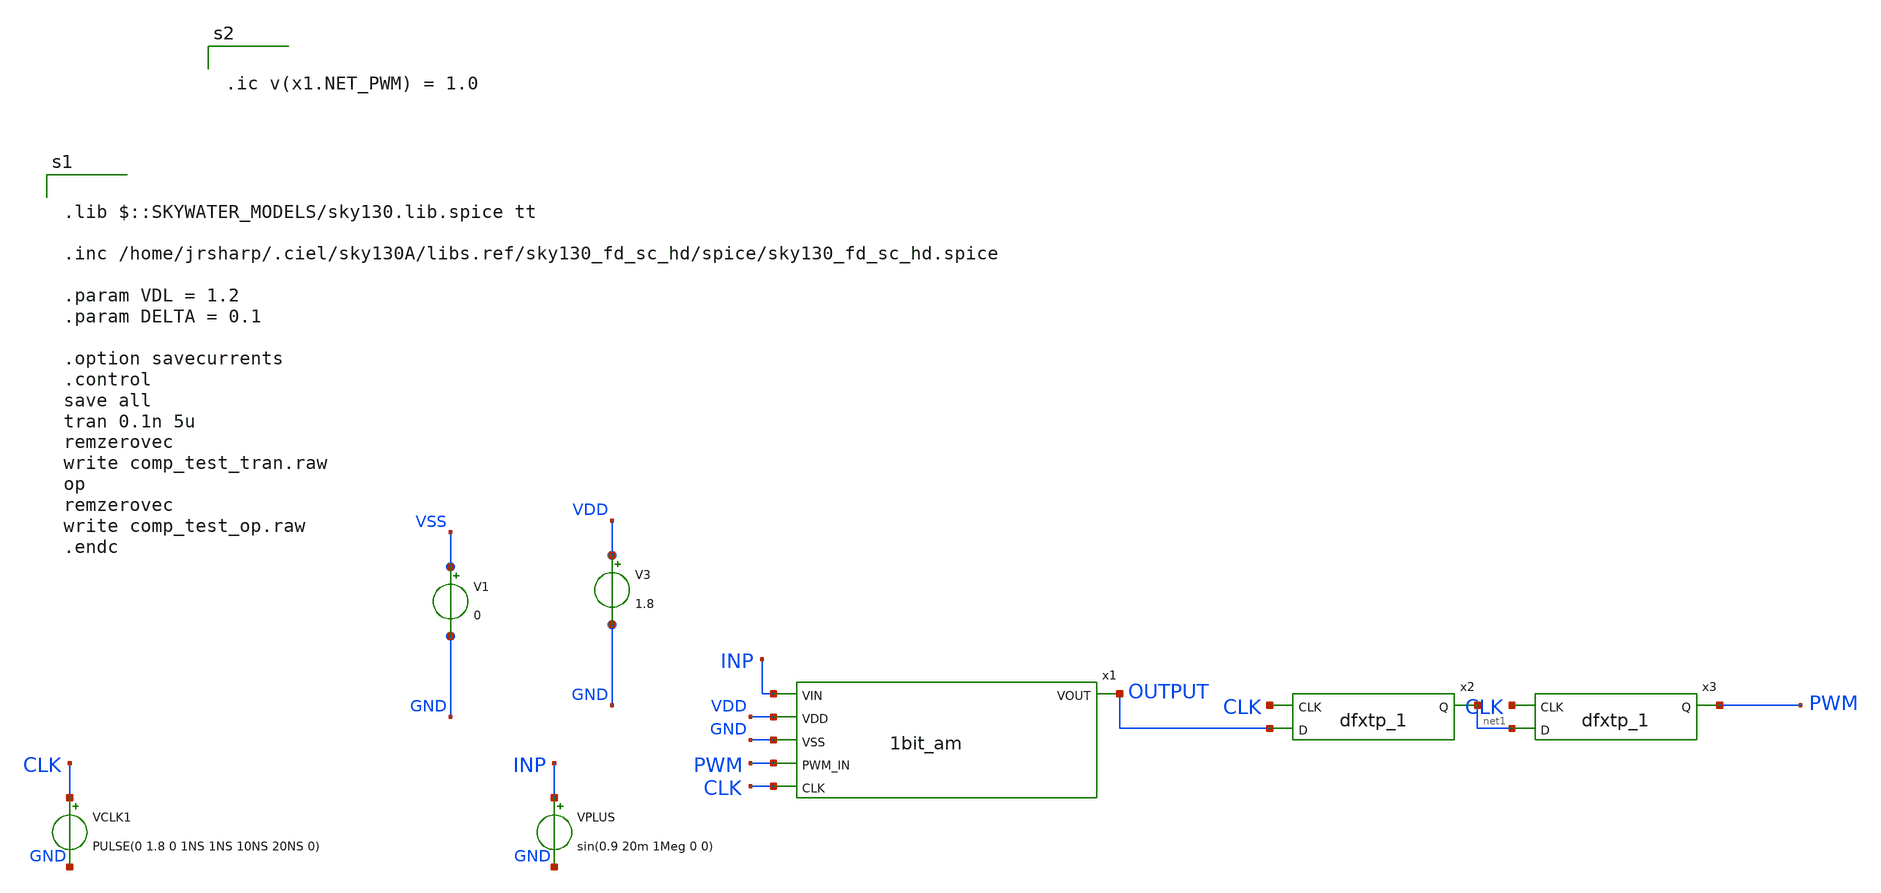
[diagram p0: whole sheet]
** sch_path: xschem/1bit_am/1bit_am_test.sch
**.subckt 1bit_am_test
x1 INP VDD GND PWM OUTPUT CLK 1bit_am
VPLUS INP GND sin(0.9 20m 1Meg 0 0)
VCLK1 CLK GND PULSE(0 1.8 0 1NS 1NS 10NS 20NS 0)
V3 VDD GND 1.8
V1 VSS GND 0
x2 CLK OUTPUT VSS VSS VDD VDD net1 sky130_fd_sc_hd__dfxtp_1
x3 CLK net1 VSS VSS VDD VDD PWM sky130_fd_sc_hd__dfxtp_1
**** begin user architecture code

.lib $::SKYWATER_MODELS/sky130.lib.spice tt

.inc /home/jrsharp/.ciel/sky130A/libs.ref/sky130_fd_sc_hd/spice/sky130_fd_sc_hd.spice

.param VDL = 1.2
.param DELTA = 0.1

.option savecurrents
.control
save all
tran 0.1n 5u
remzerovec
write comp_test_tran.raw
op
remzerovec
write comp_test_op.raw
.endc




.ic v(x1.NET_PWM) = 1.0

**** end user architecture code
**.ends

* expanding   symbol:  1bit_am.sym # of pins=6
** sym_path: xschem/1bit_am/1bit_am.sym
** sch_path: xschem/1bit_am/1bit_am.sch
.subckt 1bit_am VIN VDD VSS PWM_IN VOUT CLK
*.ipin VDD
*.ipin VSS
*.ipin CLK
*.ipin VIN
*.opin VOUT
*.ipin PWM_IN
x1 CLK NET_IN NET_PWM VDD VOUT VSS high_speed_comp_top
XR2 net2 NET_PWM net3 sky130_fd_pr__res_xhigh_po_0p35 L=30 mult=1 m=1
XR3 VDD net4 net5 sky130_fd_pr__res_xhigh_po_0p35 L=20 mult=1 m=1
XR4 net4 NET_IN net6 sky130_fd_pr__res_xhigh_po_0p35 L=20 mult=1 m=1
XR5 NET_IN net7 net8 sky130_fd_pr__res_xhigh_po_0p35 L=20 mult=1 m=1
XR6 net7 VSS net9 sky130_fd_pr__res_xhigh_po_0p35 L=20 mult=1 m=1
XC1 VIN NET_IN sky130_fd_pr__cap_mim_m3_1 W=10 L=10 MF=20 m=20
XC2 NET_PWM VSS sky130_fd_pr__cap_mim_m3_1 W=10 L=10 MF=20 m=20
x4 VSS VSS VDD VDD sky130_fd_sc_hd__decap_3
x5 VSS VSS VDD VDD sky130_fd_sc_hd__decap_3
x6 VSS VDD sky130_fd_sc_hd__tapvpwrvgnd_1
x7 VSS VDD sky130_fd_sc_hd__tapvpwrvgnd_1
XR1 net10 net11 net12 sky130_fd_pr__res_xhigh_po_0p35 L=30 mult=1 m=1
x3 PWM_IN VSS VSS VDD VDD net1 sky130_fd_sc_hd__inv_1
XR7 net11 net13 net14 sky130_fd_pr__res_xhigh_po_0p35 L=30 mult=1 m=1
XR8 net13 net2 net15 sky130_fd_pr__res_xhigh_po_0p35 L=30 mult=1 m=1
x2 net1 VSS VSS VDD VDD net10 sky130_fd_sc_hd__inv_1
.ends


* expanding   symbol:  /home/jrsharp/code/magma/xschem/flash_converter/high_speed_comp_top.sym # of
*+ pins=6
** sym_path: xschem/flash_converter/high_speed_comp_top.sym
** sch_path: xschem/flash_converter/high_speed_comp_top.sch
.subckt high_speed_comp_top CLK VINP VINN VDD COMP_OUT VSS
*.ipin VINP
*.ipin VINN
*.ipin CLK
*.opin COMP_OUT
*.ipin VDD
*.ipin VSS
x1 VDD CLK_PRIME net1 net2 VSS VINP VINN strong_arm_latch
x2 VDD net1 net2 VOUT VSS post_amplifier
x3 CLK VOUT VSS VSS VDD VDD COMP_OUT sky130_fd_sc_hd__dfxtp_2
x4 CLK VSS VSS VDD VDD CLK_PRIME sky130_fd_sc_hd__clkinv_4
x5 VSS VSS VDD VDD sky130_fd_sc_hd__decap_3
x7 VSS VSS VDD VDD sky130_fd_sc_hd__decap_3
x9 VSS VDD sky130_fd_sc_hd__tapvpwrvgnd_1
x6 VSS VDD sky130_fd_sc_hd__tapvpwrvgnd_1
x8 VSS VDD sky130_fd_sc_hd__tapvpwrvgnd_1
.ends


* expanding   symbol:  strong_arm_latch.sym # of pins=7
** sym_path: xschem/flash_converter/strong_arm_latch.sym
** sch_path: xschem/flash_converter/strong_arm_latch.sch
.subckt strong_arm_latch VDD CLK VOUT_PLUS VOUT_MINUS VSS VINP VINN
*.ipin VSS
*.ipin VDD
*.ipin CLK
*.ipin VINP
*.ipin VINN
*.opin VOUT_MINUS
*.opin VOUT_PLUS
XM1 net2 VINP net1 VSS sky130_fd_pr__nfet_01v8_lvt L=1 W=5 nf=1 ad='int((nf+1)/2) * W/nf * 0.29' as='int((nf+2)/2) * W/nf * 0.29'
+ pd='2*int((nf+1)/2) * (W/nf + 0.29)' ps='2*int((nf+2)/2) * (W/nf + 0.29)' nrd='0.29 / W' nrs='0.29 / W'
+ sa=0 sb=0 sd=0 mult=1 m=1
XM2 net3 VINN net1 VSS sky130_fd_pr__nfet_01v8_lvt L=1 W=5 nf=1 ad='int((nf+1)/2) * W/nf * 0.29' as='int((nf+2)/2) * W/nf * 0.29'
+ pd='2*int((nf+1)/2) * (W/nf + 0.29)' ps='2*int((nf+2)/2) * (W/nf + 0.29)' nrd='0.29 / W' nrs='0.29 / W'
+ sa=0 sb=0 sd=0 mult=1 m=1
XM3 net1 CLK VSS VSS sky130_fd_pr__nfet_01v8_lvt L=1 W=5 nf=1 ad='int((nf+1)/2) * W/nf * 0.29' as='int((nf+2)/2) * W/nf * 0.29'
+ pd='2*int((nf+1)/2) * (W/nf + 0.29)' ps='2*int((nf+2)/2) * (W/nf + 0.29)' nrd='0.29 / W' nrs='0.29 / W'
+ sa=0 sb=0 sd=0 mult=1 m=1
XM4 VOUT_PLUS VOUT_MINUS net2 VSS sky130_fd_pr__nfet_01v8 L=0.15 W=1 nf=1 ad='int((nf+1)/2) * W/nf * 0.29'
+ as='int((nf+2)/2) * W/nf * 0.29' pd='2*int((nf+1)/2) * (W/nf + 0.29)' ps='2*int((nf+2)/2) * (W/nf + 0.29)'
+ nrd='0.29 / W' nrs='0.29 / W' sa=0 sb=0 sd=0 mult=1 m=1
XM5 VOUT_MINUS VOUT_PLUS net3 VSS sky130_fd_pr__nfet_01v8 L=0.15 W=1 nf=1 ad='int((nf+1)/2) * W/nf * 0.29'
+ as='int((nf+2)/2) * W/nf * 0.29' pd='2*int((nf+1)/2) * (W/nf + 0.29)' ps='2*int((nf+2)/2) * (W/nf + 0.29)'
+ nrd='0.29 / W' nrs='0.29 / W' sa=0 sb=0 sd=0 mult=1 m=1
XM6 VOUT_PLUS VOUT_MINUS VDD VDD sky130_fd_pr__pfet_01v8 L=0.15 W=1 nf=1 ad='int((nf+1)/2) * W/nf * 0.29'
+ as='int((nf+2)/2) * W/nf * 0.29' pd='2*int((nf+1)/2) * (W/nf + 0.29)' ps='2*int((nf+2)/2) * (W/nf + 0.29)'
+ nrd='0.29 / W' nrs='0.29 / W' sa=0 sb=0 sd=0 mult=1 m=1
XM7 VOUT_MINUS VOUT_PLUS VDD VDD sky130_fd_pr__pfet_01v8 L=0.15 W=1 nf=1 ad='int((nf+1)/2) * W/nf * 0.29'
+ as='int((nf+2)/2) * W/nf * 0.29' pd='2*int((nf+1)/2) * (W/nf + 0.29)' ps='2*int((nf+2)/2) * (W/nf + 0.29)'
+ nrd='0.29 / W' nrs='0.29 / W' sa=0 sb=0 sd=0 mult=1 m=1
XM8 VOUT_PLUS CLK VDD VDD sky130_fd_pr__pfet_01v8 L=0.15 W=10 nf=1 ad='int((nf+1)/2) * W/nf * 0.29' as='int((nf+2)/2) * W/nf * 0.29'
+ pd='2*int((nf+1)/2) * (W/nf + 0.29)' ps='2*int((nf+2)/2) * (W/nf + 0.29)' nrd='0.29 / W' nrs='0.29 / W'
+ sa=0 sb=0 sd=0 mult=1 m=1
XM9 net2 CLK VDD VDD sky130_fd_pr__pfet_01v8 L=0.15 W=10 nf=1 ad='int((nf+1)/2) * W/nf * 0.29' as='int((nf+2)/2) * W/nf * 0.29'
+ pd='2*int((nf+1)/2) * (W/nf + 0.29)' ps='2*int((nf+2)/2) * (W/nf + 0.29)' nrd='0.29 / W' nrs='0.29 / W'
+ sa=0 sb=0 sd=0 mult=1 m=1
XM10 VOUT_MINUS CLK VDD VDD sky130_fd_pr__pfet_01v8 L=0.15 W=10 nf=1 ad='int((nf+1)/2) * W/nf * 0.29'
+ as='int((nf+2)/2) * W/nf * 0.29' pd='2*int((nf+1)/2) * (W/nf + 0.29)' ps='2*int((nf+2)/2) * (W/nf + 0.29)'
+ nrd='0.29 / W' nrs='0.29 / W' sa=0 sb=0 sd=0 mult=1 m=1
XM11 net3 CLK VDD VDD sky130_fd_pr__pfet_01v8 L=0.15 W=10 nf=1 ad='int((nf+1)/2) * W/nf * 0.29' as='int((nf+2)/2) * W/nf * 0.29'
+ pd='2*int((nf+1)/2) * (W/nf + 0.29)' ps='2*int((nf+2)/2) * (W/nf + 0.29)' nrd='0.29 / W' nrs='0.29 / W'
+ sa=0 sb=0 sd=0 mult=1 m=1
.ends


* expanding   symbol:  post_amplifier.sym # of pins=5
** sym_path: xschem/flash_converter/post_amplifier.sym
** sch_path: xschem/flash_converter/post_amplifier.sch
.subckt post_amplifier VDD VLAT_PLUS VLAT_MINUS VOUT VSS
*.ipin VLAT_PLUS
*.ipin VLAT_MINUS
*.ipin VDD
*.ipin VSS
*.opin VOUT
XM1 net1 VLAT_PLUS net4 VSS sky130_fd_pr__nfet_01v8 L=0.15 W=1 nf=1 ad='int((nf+1)/2) * W/nf * 0.29'
+ as='int((nf+2)/2) * W/nf * 0.29' pd='2*int((nf+1)/2) * (W/nf + 0.29)' ps='2*int((nf+2)/2) * (W/nf + 0.29)'
+ nrd='0.29 / W' nrs='0.29 / W' sa=0 sb=0 sd=0 mult=1 m=1
XM2 net3 VLAT_MINUS net4 VSS sky130_fd_pr__nfet_01v8 L=0.15 W=1 nf=1 ad='int((nf+1)/2) * W/nf * 0.29'
+ as='int((nf+2)/2) * W/nf * 0.29' pd='2*int((nf+1)/2) * (W/nf + 0.29)' ps='2*int((nf+2)/2) * (W/nf + 0.29)'
+ nrd='0.29 / W' nrs='0.29 / W' sa=0 sb=0 sd=0 mult=1 m=1
XM3 net4 net1 VSS VSS sky130_fd_pr__nfet_01v8 L=0.15 W=1 nf=1 ad='int((nf+1)/2) * W/nf * 0.29' as='int((nf+2)/2) * W/nf * 0.29'
+ pd='2*int((nf+1)/2) * (W/nf + 0.29)' ps='2*int((nf+2)/2) * (W/nf + 0.29)' nrd='0.29 / W' nrs='0.29 / W'
+ sa=0 sb=0 sd=0 mult=1 m=1
XM4 net1 VLAT_PLUS net2 VDD sky130_fd_pr__pfet_01v8 L=0.15 W=1 nf=1 ad='int((nf+1)/2) * W/nf * 0.29'
+ as='int((nf+2)/2) * W/nf * 0.29' pd='2*int((nf+1)/2) * (W/nf + 0.29)' ps='2*int((nf+2)/2) * (W/nf + 0.29)'
+ nrd='0.29 / W' nrs='0.29 / W' sa=0 sb=0 sd=0 mult=1 m=1
XM5 net3 VLAT_MINUS net2 VDD sky130_fd_pr__pfet_01v8 L=0.15 W=1 nf=1 ad='int((nf+1)/2) * W/nf * 0.29'
+ as='int((nf+2)/2) * W/nf * 0.29' pd='2*int((nf+1)/2) * (W/nf + 0.29)' ps='2*int((nf+2)/2) * (W/nf + 0.29)'
+ nrd='0.29 / W' nrs='0.29 / W' sa=0 sb=0 sd=0 mult=1 m=1
XM6 net2 net1 VDD VDD sky130_fd_pr__pfet_01v8 L=0.15 W=1 nf=1 ad='int((nf+1)/2) * W/nf * 0.29' as='int((nf+2)/2) * W/nf * 0.29'
+ pd='2*int((nf+1)/2) * (W/nf + 0.29)' ps='2*int((nf+2)/2) * (W/nf + 0.29)' nrd='0.29 / W' nrs='0.29 / W'
+ sa=0 sb=0 sd=0 mult=1 m=1
XM7 VOUT net3 VSS VSS sky130_fd_pr__nfet_01v8 L=0.15 W=1 nf=1 ad='int((nf+1)/2) * W/nf * 0.29' as='int((nf+2)/2) * W/nf * 0.29'
+ pd='2*int((nf+1)/2) * (W/nf + 0.29)' ps='2*int((nf+2)/2) * (W/nf + 0.29)' nrd='0.29 / W' nrs='0.29 / W'
+ sa=0 sb=0 sd=0 mult=1 m=1
XM8 VOUT net3 VDD VDD sky130_fd_pr__pfet_01v8 L=0.15 W=1 nf=1 ad='int((nf+1)/2) * W/nf * 0.29' as='int((nf+2)/2) * W/nf * 0.29'
+ pd='2*int((nf+1)/2) * (W/nf + 0.29)' ps='2*int((nf+2)/2) * (W/nf + 0.29)' nrd='0.29 / W' nrs='0.29 / W'
+ sa=0 sb=0 sd=0 mult=1 m=1
.ends

.end
